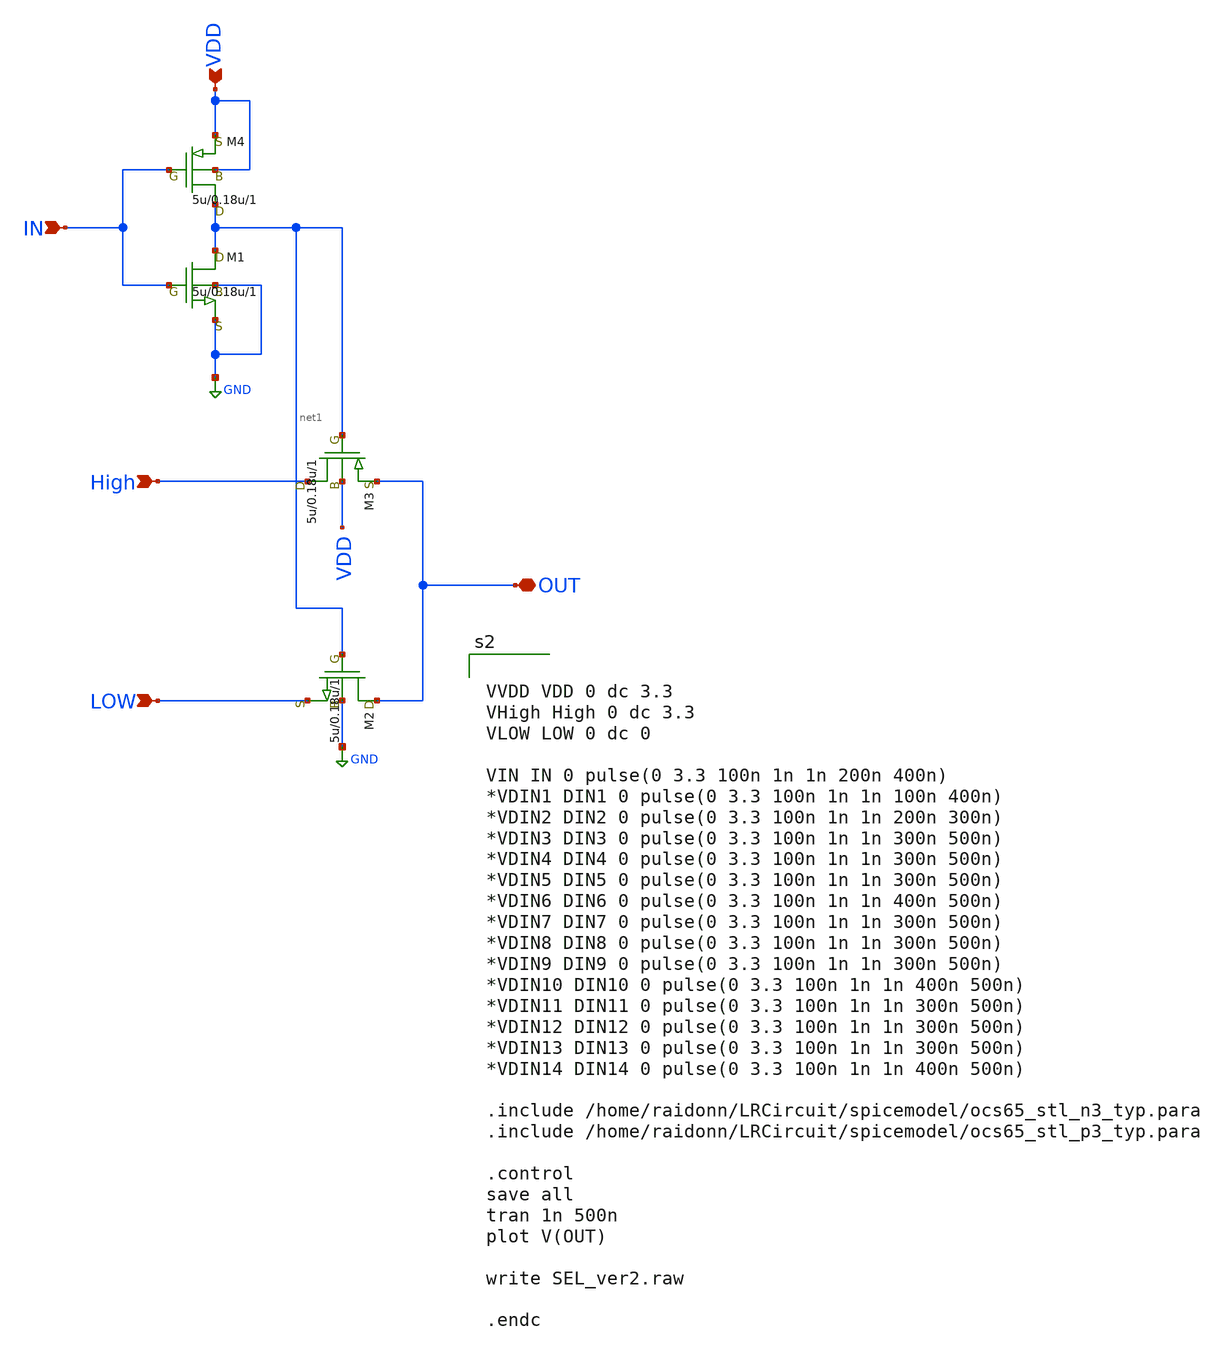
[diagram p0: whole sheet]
** sch_path: LR_Work3/SEL_ver2.sch
**.subckt SEL_ver2 High LOW IN VDD OUT
*.ipin High
*.ipin LOW
*.ipin IN
*.ipin VDD
*.iopin OUT
M4 net1 IN VDD VDD p3.0 w=5u l=0.18u as=0 ps=0 ad=0 pd=0 m=1
M1 net1 IN GND GND n3.0 w=5u l=0.18u as=0 ps=0 ad=0 pd=0 m=1
M2 OUT net1 LOW GND n3.0 w=5u l=0.18u as=0 ps=0 ad=0 pd=0 m=1
M3 High net1 OUT VDD p3.0 w=5u l=0.18u as=0 ps=0 ad=0 pd=0 m=1
**** begin user architecture code


VVDD VDD 0 dc 3.3
VHigh High 0 dc 3.3
VLOW LOW 0 dc 0

VIN IN 0 pulse(0 3.3 100n 1n 1n 200n 400n)
*VDIN1 DIN1 0 pulse(0 3.3 100n 1n 1n 100n 400n)
*VDIN2 DIN2 0 pulse(0 3.3 100n 1n 1n 200n 300n)
*VDIN3 DIN3 0 pulse(0 3.3 100n 1n 1n 300n 500n)
*VDIN4 DIN4 0 pulse(0 3.3 100n 1n 1n 300n 500n)
*VDIN5 DIN5 0 pulse(0 3.3 100n 1n 1n 300n 500n)
*VDIN6 DIN6 0 pulse(0 3.3 100n 1n 1n 400n 500n)
*VDIN7 DIN7 0 pulse(0 3.3 100n 1n 1n 300n 500n)
*VDIN8 DIN8 0 pulse(0 3.3 100n 1n 1n 300n 500n)
*VDIN9 DIN9 0 pulse(0 3.3 100n 1n 1n 300n 500n)
*VDIN10 DIN10 0 pulse(0 3.3 100n 1n 1n 400n 500n)
*VDIN11 DIN11 0 pulse(0 3.3 100n 1n 1n 300n 500n)
*VDIN12 DIN12 0 pulse(0 3.3 100n 1n 1n 300n 500n)
*VDIN13 DIN13 0 pulse(0 3.3 100n 1n 1n 300n 500n)
*VDIN14 DIN14 0 pulse(0 3.3 100n 1n 1n 400n 500n)

.include /home/raidonn/LRCircuit/spicemodel/ocs65_stl_n3_typ.para
.include /home/raidonn/LRCircuit/spicemodel/ocs65_stl_p3_typ.para

.control
save all
tran 1n 500n
plot V(OUT)

write SEL_ver2.raw

.endc

**** end user architecture code
**.ends
.GLOBAL GND
.end
